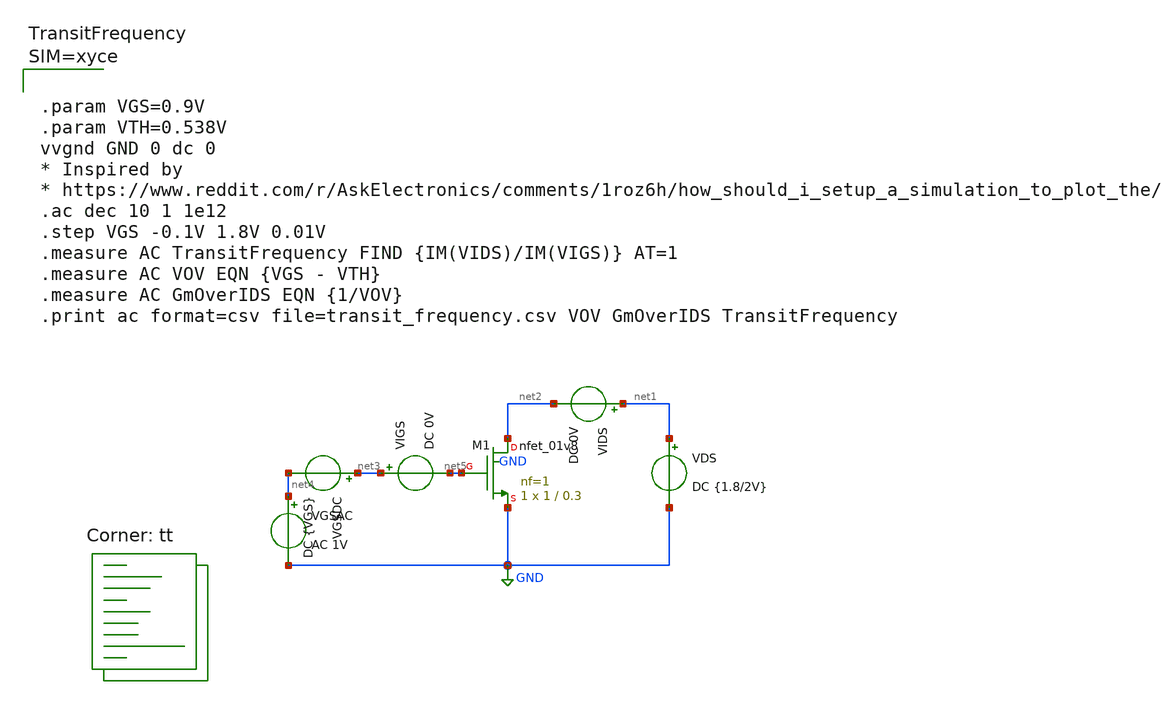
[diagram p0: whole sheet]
** sch_path: sky130/xschem/transit-frequency.sch
**.subckt transit-frequency
XM1 net2 net5 GND GND sky130_fd_pr__nfet_01v8 L=0.3 W=1 nf=1 ad='int((nf+1)/2) * W/nf * 0.29' as='int((nf+2)/2) * W/nf * 0.29'
+ pd='2*int((nf+1)/2) * (W/nf + 0.29)' ps='2*int((nf+2)/2) * (W/nf + 0.29)' nrd='0.29 / W' nrs='0.29 / W'
+ sa=0 sb=0 sd=0 mult=1 m=1
VDS net1 GND DC {1.8/2V}
VGSDC net3 net4 DC {VGS}
VGSAC net4 GND AC 1V
VIDS net1 net2 DC 0V
VIGS net3 net5 DC 0V
**** begin user architecture code
.lib $::SKYWATER_MODELS/sky130.lib.spice tt



**** end user architecture code
**.ends
.GLOBAL GND
.end
